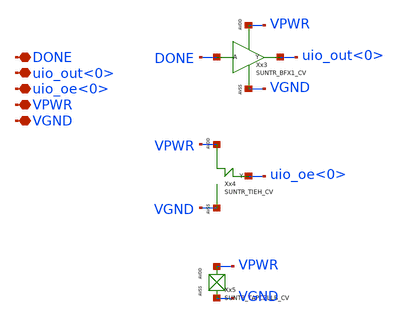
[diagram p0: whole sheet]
** sch_path: ip/tt06_sar_sky130nm/design/TT06_SAR_SKY130NM/tt_um_TT06_SAR_done.sch
**.subckt tt_um_TT06_SAR_done DONE uio_out<0> uio_oe<0> VPWR VGND
*.iopin DONE
*.iopin uio_out<0>
*.iopin uio_oe<0>
*.iopin VPWR
*.iopin VGND
Xx5 VPWR VGND SUNTR_TAPCELLB_CV xoffset=0 yoffset=0 angle=0
**.ends
.end
